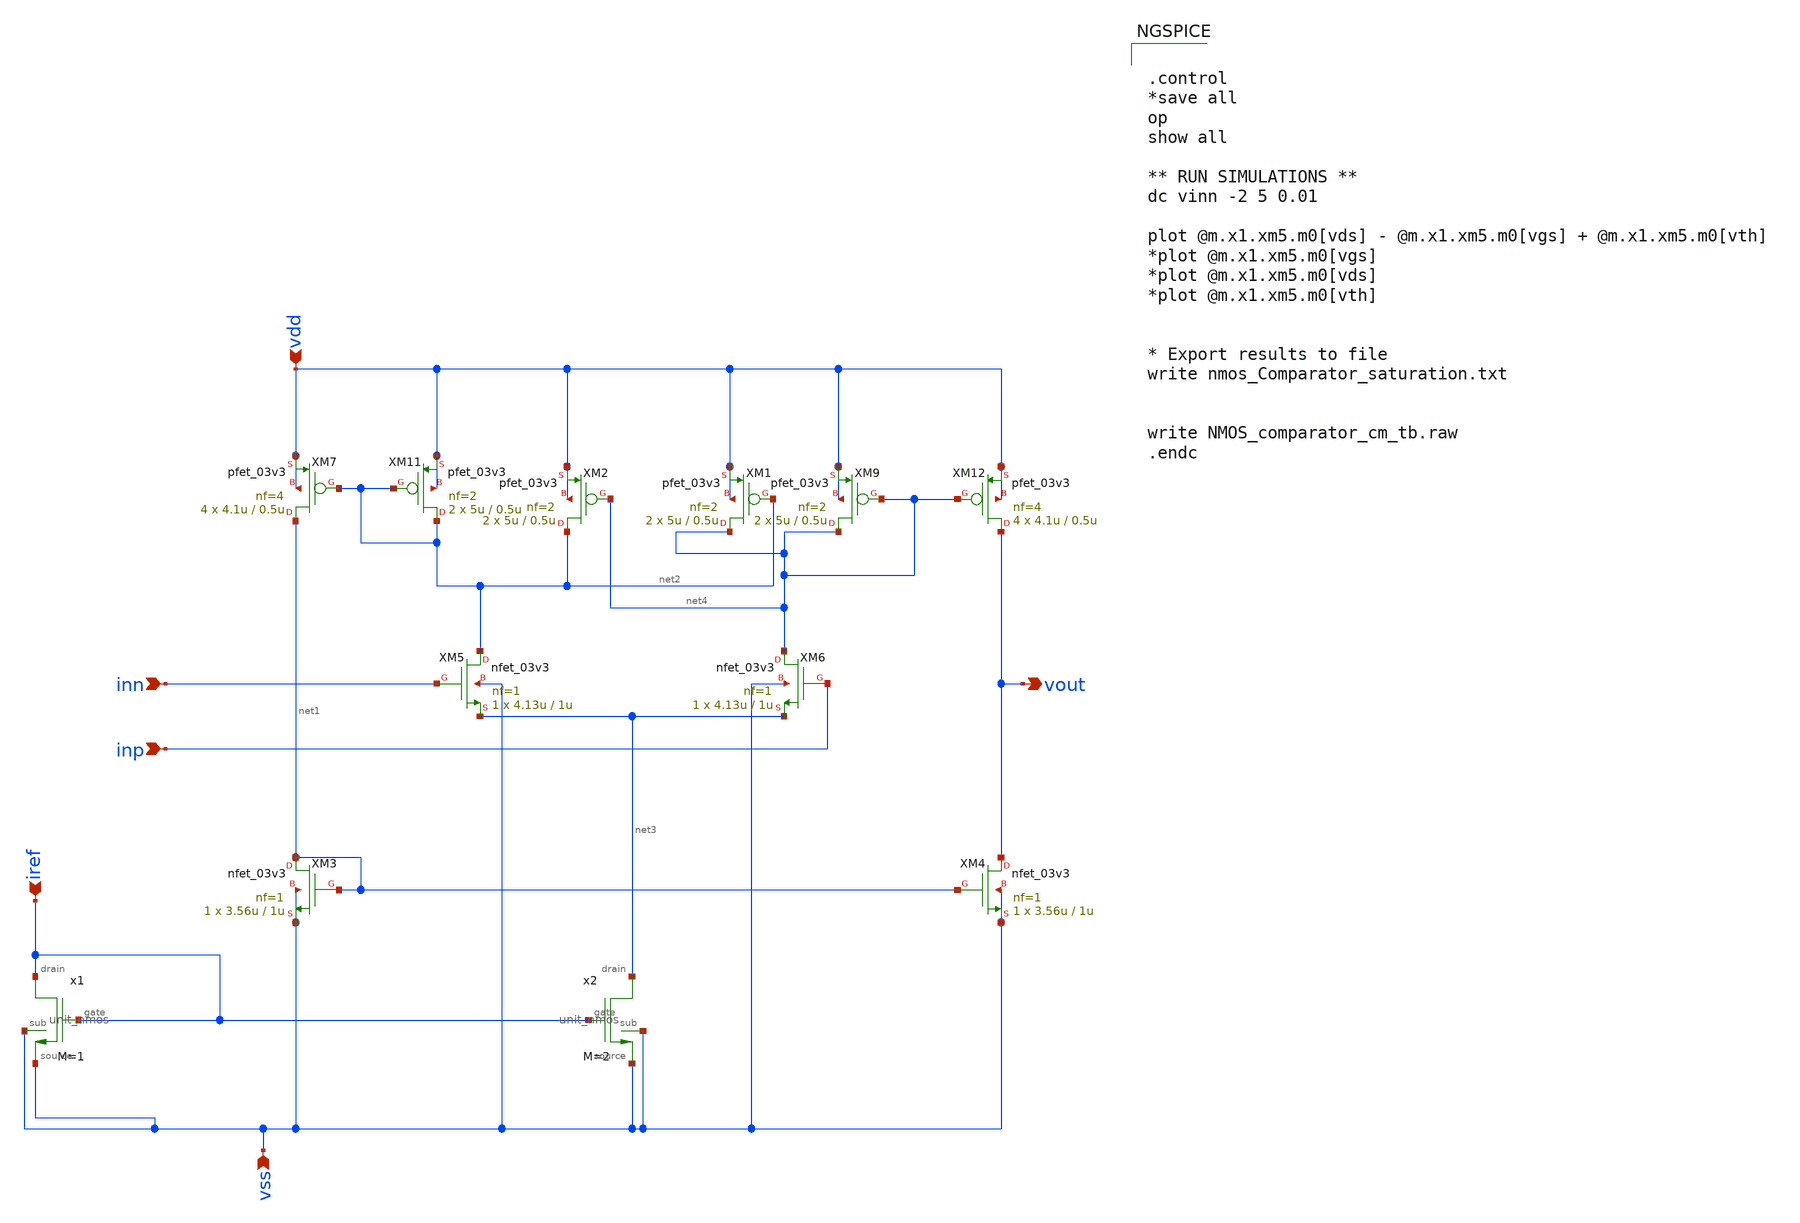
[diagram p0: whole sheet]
** sch_path: designs/libs/core_analog/Comparator/Nmos_Comparator.sch
**.subckt Nmos_Comparator vss vdd iref inn inp vout
*.ipin vss
*.ipin vdd
*.ipin iref
*.ipin inn
*.ipin inp
*.opin vout
XM3 net1 net1 vss vss nfet_03v3 L=1u W=3.56u nf=1 ad='int((nf+1)/2) * W/nf * 0.18u' as='int((nf+2)/2) * W/nf * 0.18u'
+ pd='2*int((nf+1)/2) * (W/nf + 0.18u)' ps='2*int((nf+2)/2) * (W/nf + 0.18u)' nrd='0.18u / W' nrs='0.18u / W'
+ sa=0 sb=0 sd=0 m=1
XM4 vout net1 vss vss nfet_03v3 L=1u W=3.56u nf=1 ad='int((nf+1)/2) * W/nf * 0.18u' as='int((nf+2)/2) * W/nf * 0.18u'
+ pd='2*int((nf+1)/2) * (W/nf + 0.18u)' ps='2*int((nf+2)/2) * (W/nf + 0.18u)' nrd='0.18u / W' nrs='0.18u / W'
+ sa=0 sb=0 sd=0 m=1
XM5 net2 inn net3 vss nfet_03v3 L=1u W=4.13u nf=1 ad='int((nf+1)/2) * W/nf * 0.18u' as='int((nf+2)/2) * W/nf * 0.18u'
+ pd='2*int((nf+1)/2) * (W/nf + 0.18u)' ps='2*int((nf+2)/2) * (W/nf + 0.18u)' nrd='0.18u / W' nrs='0.18u / W'
+ sa=0 sb=0 sd=0 m=1
XM6 net4 inp net3 vss nfet_03v3 L=1u W=4.13u nf=1 ad='int((nf+1)/2) * W/nf * 0.18u' as='int((nf+2)/2) * W/nf * 0.18u'
+ pd='2*int((nf+1)/2) * (W/nf + 0.18u)' ps='2*int((nf+2)/2) * (W/nf + 0.18u)' nrd='0.18u / W' nrs='0.18u / W'
+ sa=0 sb=0 sd=0 m=1
XM7 net1 net2 vdd vdd pfet_03v3 L=0.5u W=4.1u nf=4 ad='int((nf+1)/2) * W/nf * 0.18u' as='int((nf+2)/2) * W/nf * 0.18u'
+ pd='2*int((nf+1)/2) * (W/nf + 0.18u)' ps='2*int((nf+2)/2) * (W/nf + 0.18u)' nrd='0.18u / W' nrs='0.18u / W'
+ sa=0 sb=0 sd=0 m=4
XM9 net4 net4 vdd vdd pfet_03v3 L=0.5u W=5u nf=2 ad='int((nf+1)/2) * W/nf * 0.18u' as='int((nf+2)/2) * W/nf * 0.18u'
+ pd='2*int((nf+1)/2) * (W/nf + 0.18u)' ps='2*int((nf+2)/2) * (W/nf + 0.18u)' nrd='0.18u / W' nrs='0.18u / W'
+ sa=0 sb=0 sd=0 m=2
XM11 net2 net2 vdd vdd pfet_03v3 L=0.5u W=5u nf=2 ad='int((nf+1)/2) * W/nf * 0.18u' as='int((nf+2)/2) * W/nf * 0.18u'
+ pd='2*int((nf+1)/2) * (W/nf + 0.18u)' ps='2*int((nf+2)/2) * (W/nf + 0.18u)' nrd='0.18u / W' nrs='0.18u / W'
+ sa=0 sb=0 sd=0 m=2
XM12 vout net4 vdd vdd pfet_03v3 L=0.5u W=4.1u nf=4 ad='int((nf+1)/2) * W/nf * 0.18u' as='int((nf+2)/2) * W/nf * 0.18u'
+ pd='2*int((nf+1)/2) * (W/nf + 0.18u)' ps='2*int((nf+2)/2) * (W/nf + 0.18u)' nrd='0.18u / W' nrs='0.18u / W'
+ sa=0 sb=0 sd=0 m=4
x1 iref vss iref vss unit_nmos M=1
x2 net3 vss iref vss unit_nmos M=2
XM1 net4 net2 vdd vdd pfet_03v3 L=0.5u W=5u nf=2 ad='int((nf+1)/2) * W/nf * 0.18u' as='int((nf+2)/2) * W/nf * 0.18u'
+ pd='2*int((nf+1)/2) * (W/nf + 0.18u)' ps='2*int((nf+2)/2) * (W/nf + 0.18u)' nrd='0.18u / W' nrs='0.18u / W'
+ sa=0 sb=0 sd=0 m=2
XM2 net2 net4 vdd vdd pfet_03v3 L=0.5u W=5u nf=2 ad='int((nf+1)/2) * W/nf * 0.18u' as='int((nf+2)/2) * W/nf * 0.18u'
+ pd='2*int((nf+1)/2) * (W/nf + 0.18u)' ps='2*int((nf+2)/2) * (W/nf + 0.18u)' nrd='0.18u / W' nrs='0.18u / W'
+ sa=0 sb=0 sd=0 m=2
**** begin user architecture code


.control
*save all
op
show all

** RUN SIMULATIONS **
dc vinn -2 5 0.01

plot @m.x1.xm5.m0[vds] - @m.x1.xm5.m0[vgs] + @m.x1.xm5.m0[vth]
*plot @m.x1.xm5.m0[vgs]
*plot @m.x1.xm5.m0[vds]
*plot @m.x1.xm5.m0[vth]


* Export results to file
write nmos_Comparator_saturation.txt


write NMOS_comparator_cm_tb.raw
.endc


**** end user architecture code
**.ends

* expanding   symbol:  libs/core_analog/unit_nmos/unit_nmos.sym # of pins=4
** sym_path: libs/core_analog/unit_nmos/unit_nmos.sym
** sch_path: libs/core_analog/unit_nmos/unit_nmos.sch
.subckt unit_nmos drain sub gate source
*.iopin drain
*.iopin source
*.iopin sub
*.iopin gate
XM1 drain gate source sub nfet_03v3 L=1u W=2.5u nf=1 ad='int((nf+1)/2) * W/nf * 0.18u' as='int((nf+2)/2) * W/nf * 0.18u'
+ pd='2*int((nf+1)/2) * (W/nf + 0.18u)' ps='2*int((nf+2)/2) * (W/nf + 0.18u)' nrd='0.18u / W' nrs='0.18u / W'
+ sa=0 sb=0 sd=0 m={M}
**** begin user architecture code

.param M=1

**** end user architecture code
.ends

.end
